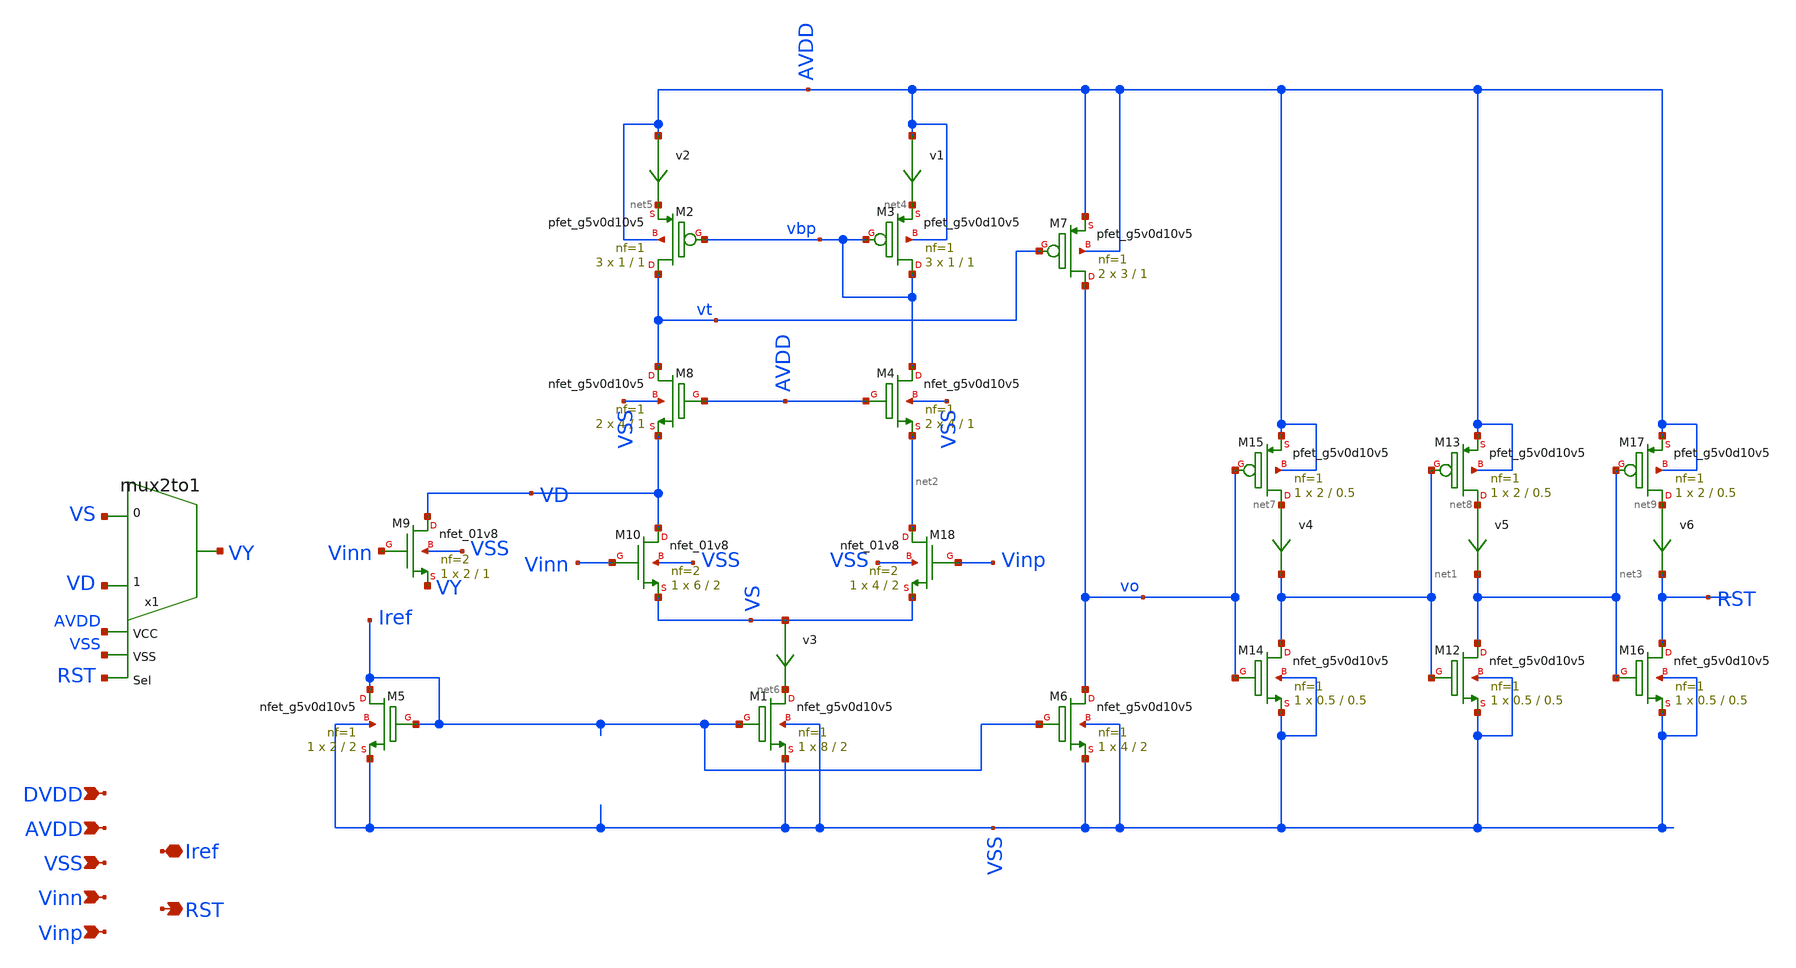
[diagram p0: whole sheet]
** sch_path: xschem_sim/comparator_v2.sch
**.subckt comparator_v2 AVDD RST VSS Iref Vinn Vinp DVDD
*.ipin AVDD
*.opin RST
*.ipin VSS
*.iopin Iref
*.ipin Vinn
*.ipin Vinp
*.ipin DVDD
v1 AVDD net4 0
.save i(v1)
v2 AVDD net5 0
.save i(v2)
XM1 net6 Iref VSS VSS sky130_fd_pr__nfet_g5v0d10v5 L=2 W=8 nf=1 ad='int((nf+1)/2) * W/nf * 0.29' as='int((nf+2)/2) * W/nf * 0.29'
+ pd='2*int((nf+1)/2) * (W/nf + 0.29)' ps='2*int((nf+2)/2) * (W/nf + 0.29)' nrd='0.29 / W' nrs='0.29 / W'
+ sa=0 sb=0 sd=0 mult=1 m=1
XM3 vbp vbp net4 AVDD sky130_fd_pr__pfet_g5v0d10v5 L=1 W=1 nf=1 ad='int((nf+1)/2) * W/nf * 0.29' as='int((nf+2)/2) * W/nf * 0.29'
+ pd='2*int((nf+1)/2) * (W/nf + 0.29)' ps='2*int((nf+2)/2) * (W/nf + 0.29)' nrd='0.29 / W' nrs='0.29 / W'
+ sa=0 sb=0 sd=0 mult=3 m=3
XM2 vt vbp net5 AVDD sky130_fd_pr__pfet_g5v0d10v5 L=1 W=1 nf=1 ad='int((nf+1)/2) * W/nf * 0.29' as='int((nf+2)/2) * W/nf * 0.29'
+ pd='2*int((nf+1)/2) * (W/nf + 0.29)' ps='2*int((nf+2)/2) * (W/nf + 0.29)' nrd='0.29 / W' nrs='0.29 / W'
+ sa=0 sb=0 sd=0 mult=3 m=3
v4 net7 net1 0
.save i(v4)
XM5 Iref Iref VSS VSS sky130_fd_pr__nfet_g5v0d10v5 L=2 W=2 nf=1 ad='int((nf+1)/2) * W/nf * 0.29' as='int((nf+2)/2) * W/nf * 0.29'
+ pd='2*int((nf+1)/2) * (W/nf + 0.29)' ps='2*int((nf+2)/2) * (W/nf + 0.29)' nrd='0.29 / W' nrs='0.29 / W'
+ sa=0 sb=0 sd=0 mult=1 m=1
XM7 vo vt AVDD AVDD sky130_fd_pr__pfet_g5v0d10v5 L=1 W=3 nf=1 ad='int((nf+1)/2) * W/nf * 0.29' as='int((nf+2)/2) * W/nf * 0.29'
+ pd='2*int((nf+1)/2) * (W/nf + 0.29)' ps='2*int((nf+2)/2) * (W/nf + 0.29)' nrd='0.29 / W' nrs='0.29 / W'
+ sa=0 sb=0 sd=0 mult=2 m=2
v3 VS net6 0
.save i(v3)
x1 VD VS VY AVDD VSS RST mux2to1
XM6 vo Iref VSS VSS sky130_fd_pr__nfet_g5v0d10v5 L=2 W=4 nf=1 ad='int((nf+1)/2) * W/nf * 0.29' as='int((nf+2)/2) * W/nf * 0.29'
+ pd='2*int((nf+1)/2) * (W/nf + 0.29)' ps='2*int((nf+2)/2) * (W/nf + 0.29)' nrd='0.29 / W' nrs='0.29 / W'
+ sa=0 sb=0 sd=0 mult=1 m=1
XM14 net1 vo VSS VSS sky130_fd_pr__nfet_g5v0d10v5 L=0.5 W=0.5 nf=1 ad='int((nf+1)/2) * W/nf * 0.29' as='int((nf+2)/2) * W/nf * 0.29'
+ pd='2*int((nf+1)/2) * (W/nf + 0.29)' ps='2*int((nf+2)/2) * (W/nf + 0.29)' nrd='0.29 / W' nrs='0.29 / W'
+ sa=0 sb=0 sd=0 mult=1 m=1
XM15 net7 vo AVDD AVDD sky130_fd_pr__pfet_g5v0d10v5 L=0.5 W=2 nf=1 ad='int((nf+1)/2) * W/nf * 0.29' as='int((nf+2)/2) * W/nf * 0.29'
+ pd='2*int((nf+1)/2) * (W/nf + 0.29)' ps='2*int((nf+2)/2) * (W/nf + 0.29)' nrd='0.29 / W' nrs='0.29 / W'
+ sa=0 sb=0 sd=0 mult=1 m=1
XM4 vbp AVDD net2 VSS sky130_fd_pr__nfet_g5v0d10v5 L=1 W=4 nf=1 ad='int((nf+1)/2) * W/nf * 0.29' as='int((nf+2)/2) * W/nf * 0.29'
+ pd='2*int((nf+1)/2) * (W/nf + 0.29)' ps='2*int((nf+2)/2) * (W/nf + 0.29)' nrd='0.29 / W' nrs='0.29 / W'
+ sa=0 sb=0 sd=0 mult=2 m=2
XM8 vt AVDD VD VSS sky130_fd_pr__nfet_g5v0d10v5 L=1 W=4 nf=1 ad='int((nf+1)/2) * W/nf * 0.29' as='int((nf+2)/2) * W/nf * 0.29'
+ pd='2*int((nf+1)/2) * (W/nf + 0.29)' ps='2*int((nf+2)/2) * (W/nf + 0.29)' nrd='0.29 / W' nrs='0.29 / W'
+ sa=0 sb=0 sd=0 mult=2 m=2
v5 net8 net3 0
.save i(v5)
XM12 net3 net1 VSS VSS sky130_fd_pr__nfet_g5v0d10v5 L=0.5 W=0.5 nf=1 ad='int((nf+1)/2) * W/nf * 0.29'
+ as='int((nf+2)/2) * W/nf * 0.29' pd='2*int((nf+1)/2) * (W/nf + 0.29)' ps='2*int((nf+2)/2) * (W/nf + 0.29)'
+ nrd='0.29 / W' nrs='0.29 / W' sa=0 sb=0 sd=0 mult=1 m=1
XM13 net8 net1 AVDD AVDD sky130_fd_pr__pfet_g5v0d10v5 L=0.5 W=2 nf=1 ad='int((nf+1)/2) * W/nf * 0.29'
+ as='int((nf+2)/2) * W/nf * 0.29' pd='2*int((nf+1)/2) * (W/nf + 0.29)' ps='2*int((nf+2)/2) * (W/nf + 0.29)'
+ nrd='0.29 / W' nrs='0.29 / W' sa=0 sb=0 sd=0 mult=1 m=1
v6 net9 RST 0
.save i(v6)
XM16 RST net3 VSS VSS sky130_fd_pr__nfet_g5v0d10v5 L=0.5 W=0.5 nf=1 ad='int((nf+1)/2) * W/nf * 0.29'
+ as='int((nf+2)/2) * W/nf * 0.29' pd='2*int((nf+1)/2) * (W/nf + 0.29)' ps='2*int((nf+2)/2) * (W/nf + 0.29)'
+ nrd='0.29 / W' nrs='0.29 / W' sa=0 sb=0 sd=0 mult=1 m=1
XM17 net9 net3 AVDD AVDD sky130_fd_pr__pfet_g5v0d10v5 L=0.5 W=2 nf=1 ad='int((nf+1)/2) * W/nf * 0.29'
+ as='int((nf+2)/2) * W/nf * 0.29' pd='2*int((nf+1)/2) * (W/nf + 0.29)' ps='2*int((nf+2)/2) * (W/nf + 0.29)'
+ nrd='0.29 / W' nrs='0.29 / W' sa=0 sb=0 sd=0 mult=1 m=1
XM18 net2 Vinp VS VSS sky130_fd_pr__nfet_01v8 L=2 W=4 nf=2 ad='int((nf+1)/2) * W/nf * 0.29' as='int((nf+2)/2) * W/nf * 0.29'
+ pd='2*int((nf+1)/2) * (W/nf + 0.29)' ps='2*int((nf+2)/2) * (W/nf + 0.29)' nrd='0.29 / W' nrs='0.29 / W'
+ sa=0 sb=0 sd=0 mult=1 m=1
XM10 VD Vinn VS VSS sky130_fd_pr__nfet_01v8 L=2 W=6 nf=2 ad='int((nf+1)/2) * W/nf * 0.29' as='int((nf+2)/2) * W/nf * 0.29'
+ pd='2*int((nf+1)/2) * (W/nf + 0.29)' ps='2*int((nf+2)/2) * (W/nf + 0.29)' nrd='0.29 / W' nrs='0.29 / W'
+ sa=0 sb=0 sd=0 mult=1 m=1
XM9 VD Vinn VY VSS sky130_fd_pr__nfet_01v8 L=1 W=2 nf=2 ad='int((nf+1)/2) * W/nf * 0.29' as='int((nf+2)/2) * W/nf * 0.29'
+ pd='2*int((nf+1)/2) * (W/nf + 0.29)' ps='2*int((nf+2)/2) * (W/nf + 0.29)' nrd='0.29 / W' nrs='0.29 / W'
+ sa=0 sb=0 sd=0 mult=1 m=1
**.ends
.end
